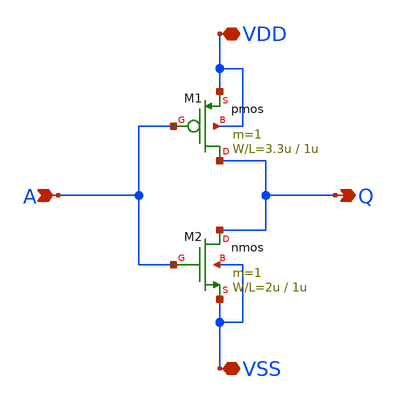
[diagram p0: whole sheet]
** sch_path: member_project/sanken/yasuike/inverter/inverter.sch
**.subckt inverter Q A VDD VSS
*.opin Q
*.ipin A
*.iopin VDD
*.iopin VSS
M1 Q A VDD VDD pmos L=1u W=3.3u m=1
M2 Q A VSS VSS nmos L=1u W=2u m=1
**.ends
.end
